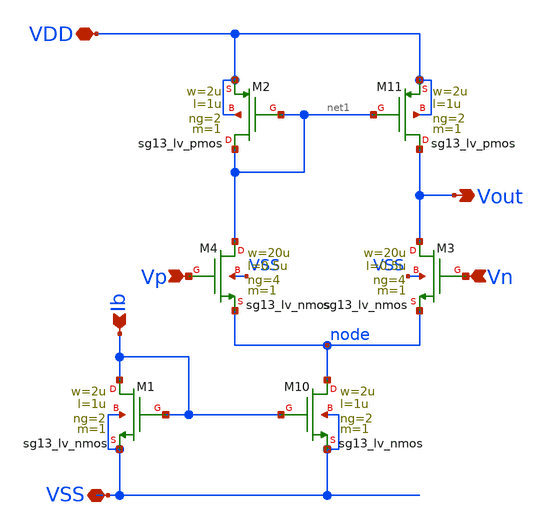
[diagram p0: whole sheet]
** sch_path: examples/sg13g2_cace_ip__ota5t/xschem/sg13g2_cace_ip__ota5t.sch
**.subckt sg13g2_cace_ip__ota5t Vp Vn Vout VDD VSS Ib
*.ipin Vp
*.ipin Vn
*.opin Vout
*.iopin VDD
*.iopin VSS
*.ipin Ib
XM10 node Ib VSS VSS sg13_lv_nmos w=2u l=1u ng=2 m=1 mm_ok=1
XM11 Vout net1 VDD VDD sg13_lv_pmos w=2u l=1u ng=2 m=1 mm_ok=1
XM1 Ib Ib VSS VSS sg13_lv_nmos w=2u l=1u ng=2 m=1 mm_ok=1
XM2 net1 net1 VDD VDD sg13_lv_pmos w=2u l=1u ng=2 m=1 mm_ok=1
XM3 Vout Vn node VSS sg13_lv_nmos w=20u l=0.5u ng=4 m=1 mm_ok=1
XM4 net1 Vp node VSS sg13_lv_nmos w=20u l=0.5u ng=4 m=1 mm_ok=1
**.ends
.end
